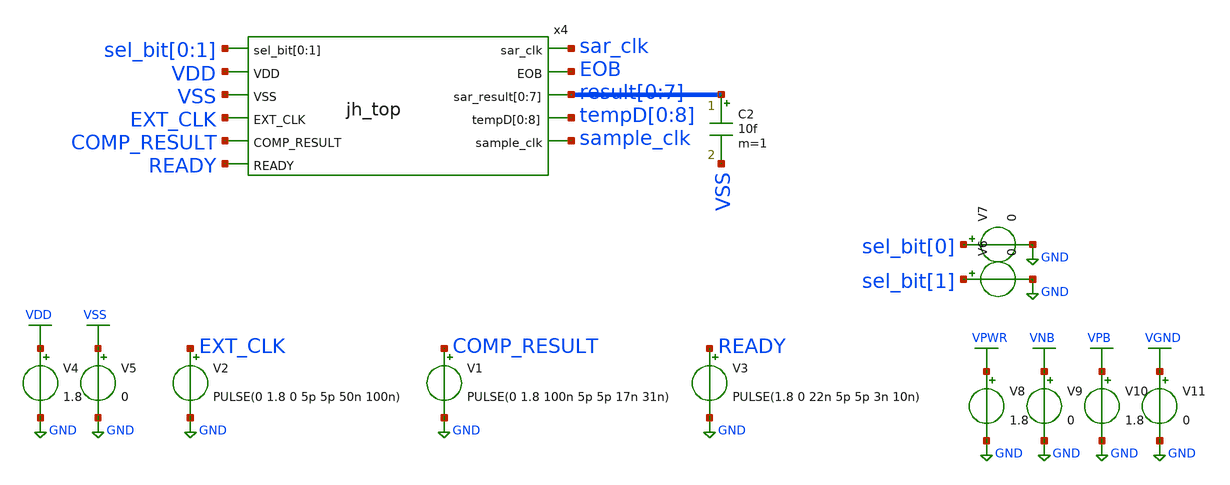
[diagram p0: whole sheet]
** sch_path: module/jh_top/tb_jh_top.sch
**.subckt tb_jh_top
V2 EXT_CLK GND PULSE(0 1.8 0 5p 5p 50n 100n)
V4 VDD GND 1.8
V1 COMP_RESULT GND PULSE(0 1.8 100n 5p 5p 17n 31n)
V5 VSS GND 0
V3 READY GND PULSE(1.8 0 22n 5p 5p 3n 10n)
x4 sel_bit[0] sel_bit[1] sar_clk VDD VSS EOB EXT_CLK result[0] result[1] result[2] result[3]
+ result[4] result[5] result[6] result[7] COMP_RESULT tempD[0] tempD[1] tempD[2] tempD[3] tempD[4] tempD[5]
+ tempD[6] tempD[7] tempD[8] sample_clk READY jh_top
C2 result[0] VSS 10f m=1
V6 sel_bit[1] GND 0
V7 sel_bit[0] GND 0
V8 VPWR GND 1.8
V9 VNB GND 0
V10 VPB GND 1.8
V11 VGND GND 0
**** begin user architecture code



.lib /foss/pdks/sky130A/libs.tech/ngspice/sky130.lib.spice tt
.include /foss/pdks/sky130A/libs.ref/sky130_fd_sc_hd/spice/sky130_fd_sc_hd.spice

.tran 1ns 600ns

.control
	run
	plot V(EXT_CLK)-2 V(sample_clk) V(EOB)+2 V(READY)+4 V(sar_clk)+6 V(COMP_RESULT)+8
	plot V("tempD[0]") V("tempD[1]")+2 V("tempD[2]")+4 V("tempD[3]")+6 V("tempD[4]")+8 V("tempD[5]")+10
+ V("tempD[6]")+12 V("tempD[7]")+14 V(sar_clk) V(sar_clk)+2 V(sar_clk)+4 V(sar_clk)+6 V(sar_clk)+8 V(sar_clk)+10
+ V(sar_clk)+12 V(sar_clk)+14 V(EOB)-2
	plot V("result[0]") V("result[1]")+2 V("result[2]")+4 V("result[3]")+6 V("result[4]")+8
+ V("result[5]")+10 V("result[6]")+12 V("result[7]")+14
 .endc
.save all



**** end user architecture code
**.ends
.GLOBAL GND
.GLOBAL VDD
.GLOBAL VSS
.GLOBAL VGND
.GLOBAL VNB
.GLOBAL VPB
.GLOBAL VPWR
.end
